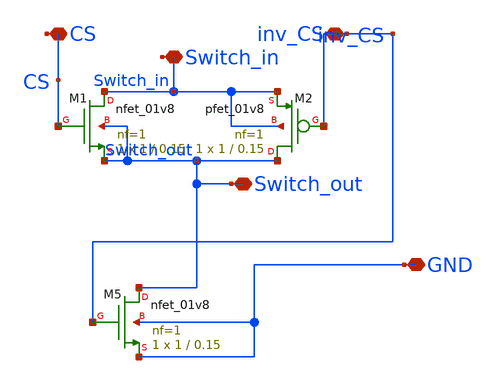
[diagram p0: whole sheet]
** sch_path: ProjectDesigns/Switch/Switch.sch
**.subckt Switch Switch_in Switch_out CS inv_CS GND
*.iopin Switch_in
*.iopin Switch_out
*.iopin CS
*.iopin inv_CS
*.iopin GND
XM1 Switch_in CS Switch_out Switch_out sky130_fd_pr__nfet_01v8 L=0.15 W=1 nf=1 ad='int((nf+1)/2) * W/nf * 0.29'
+ as='int((nf+2)/2) * W/nf * 0.29' pd='2*int((nf+1)/2) * (W/nf + 0.29)' ps='2*int((nf+2)/2) * (W/nf + 0.29)'
+ nrd='0.29 / W' nrs='0.29 / W' sa=0 sb=0 sd=0 mult=1 m=1
XM2 Switch_out inv_CS Switch_in Switch_in sky130_fd_pr__pfet_01v8 L=0.15 W=1 nf=1 ad='int((nf+1)/2) * W/nf * 0.29'
+ as='int((nf+2)/2) * W/nf * 0.29' pd='2*int((nf+1)/2) * (W/nf + 0.29)' ps='2*int((nf+2)/2) * (W/nf + 0.29)'
+ nrd='0.29 / W' nrs='0.29 / W' sa=0 sb=0 sd=0 mult=1 m=1
XM5 Switch_out inv_CS GND GND sky130_fd_pr__nfet_01v8 L=0.15 W=1 nf=1 ad='int((nf+1)/2) * W/nf * 0.29'
+ as='int((nf+2)/2) * W/nf * 0.29' pd='2*int((nf+1)/2) * (W/nf + 0.29)' ps='2*int((nf+2)/2) * (W/nf + 0.29)'
+ nrd='0.29 / W' nrs='0.29 / W' sa=0 sb=0 sd=0 mult=1 m=1
**.ends
.end
